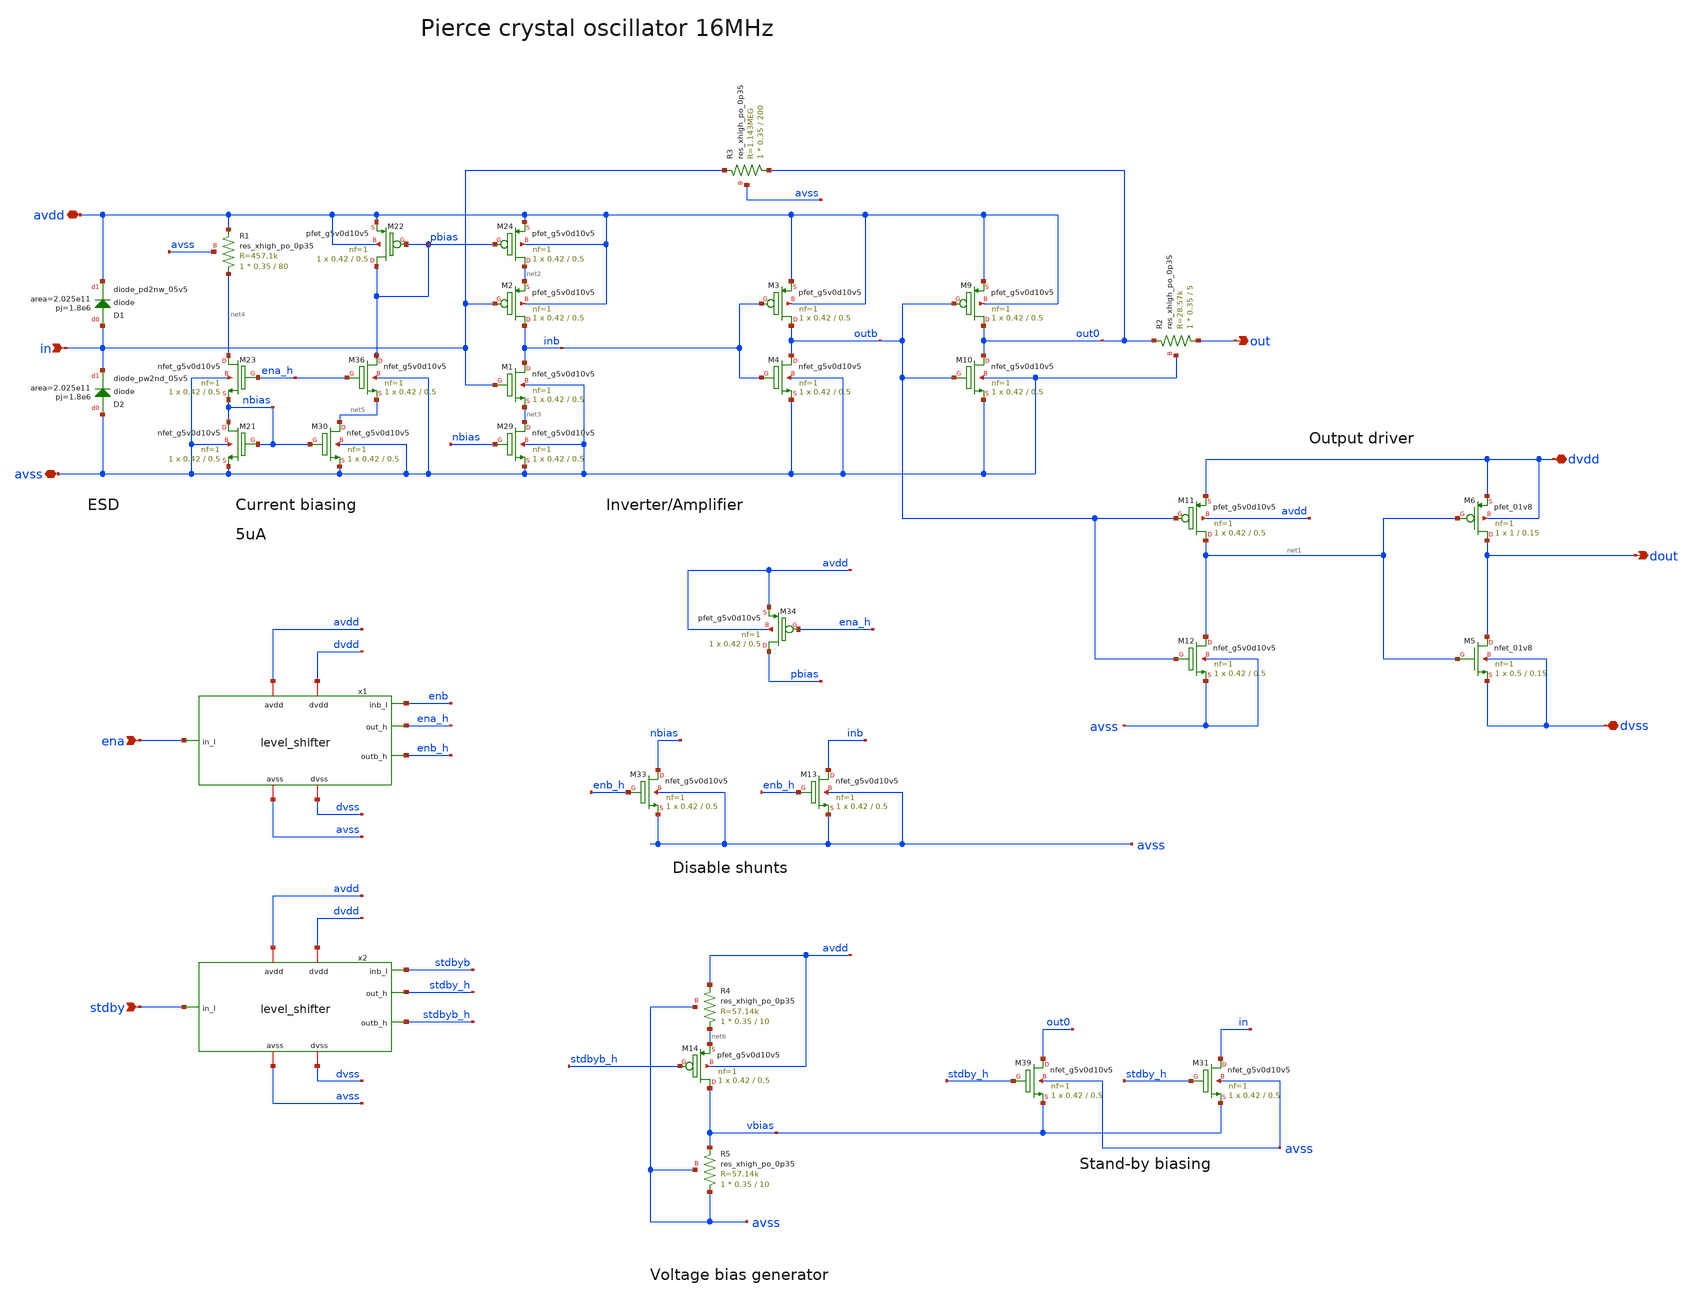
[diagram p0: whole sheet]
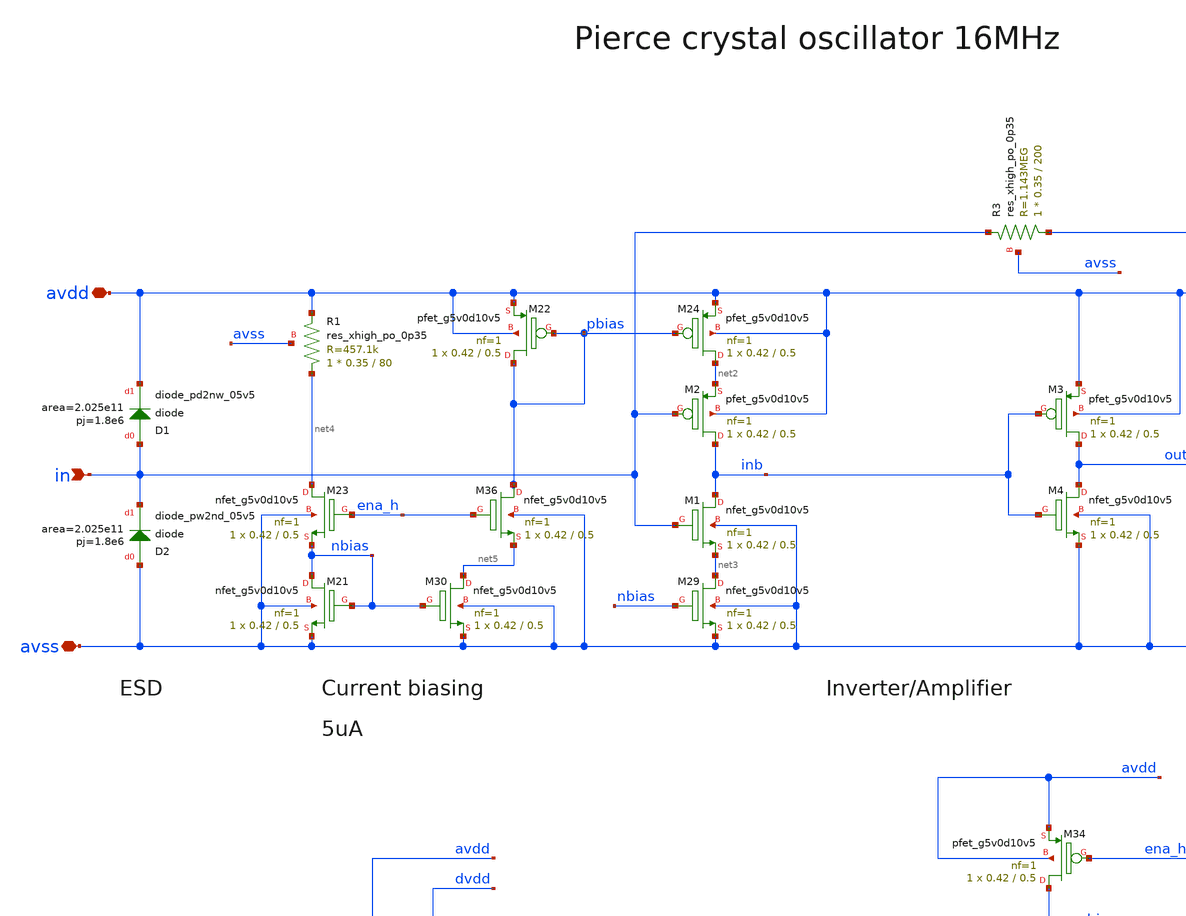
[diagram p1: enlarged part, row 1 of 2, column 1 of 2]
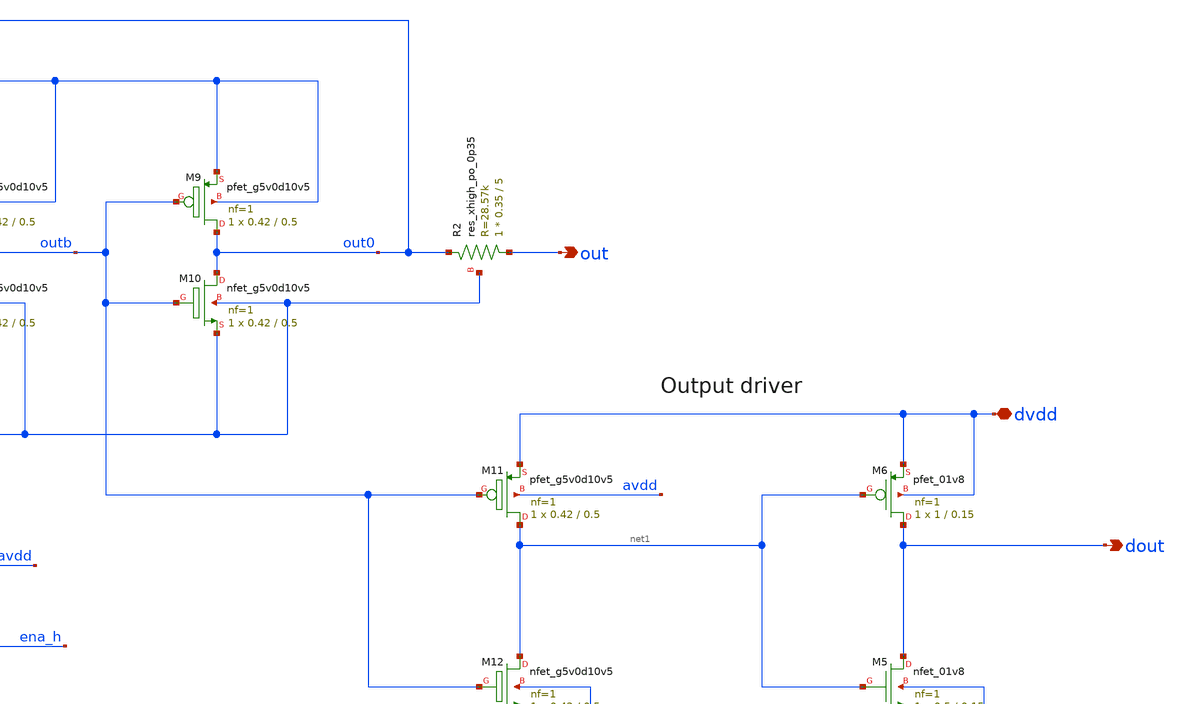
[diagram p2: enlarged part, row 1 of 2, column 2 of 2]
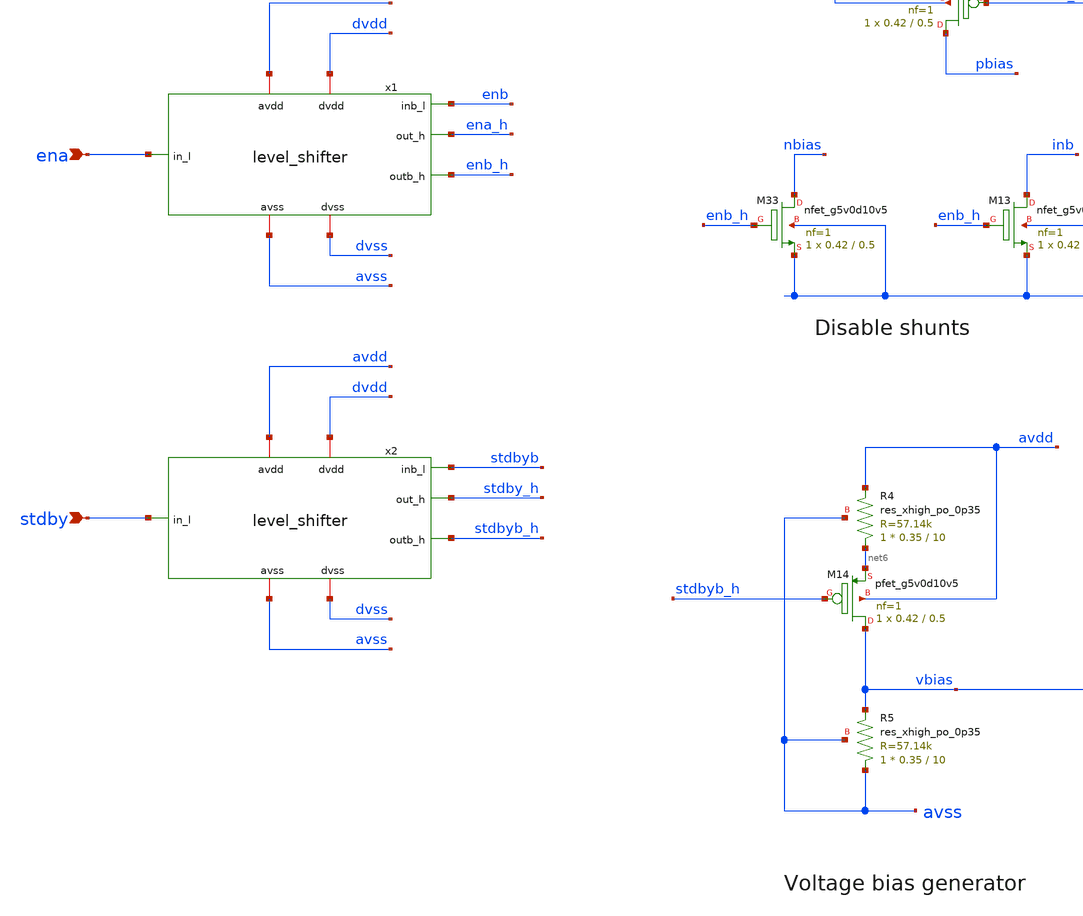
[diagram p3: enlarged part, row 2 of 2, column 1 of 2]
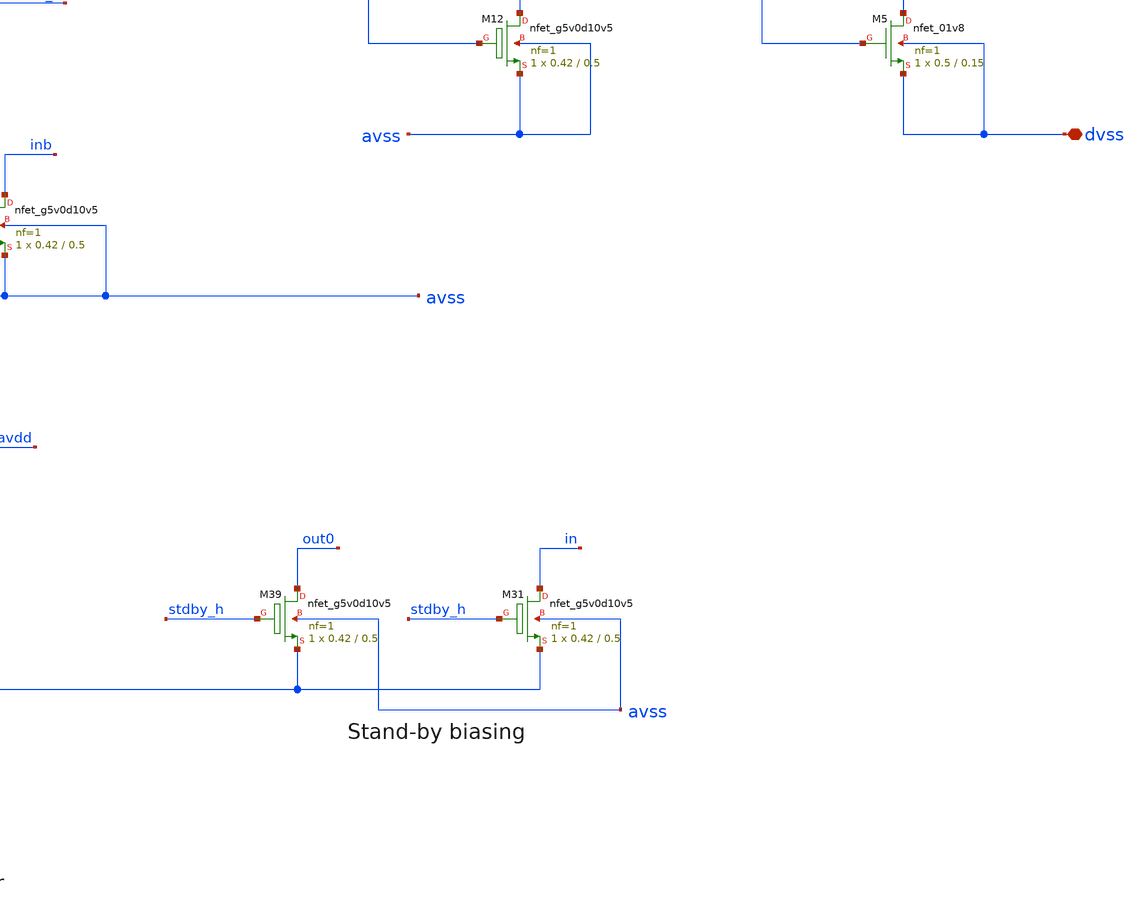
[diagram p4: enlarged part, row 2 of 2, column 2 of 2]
** sch_path: xschem/sky130_ef_ip__xtal_osc_16M.sch
**.subckt sky130_ef_ip__xtal_osc_16M in out avdd avss dvss dvdd ena dout stdby
*.ipin in
*.opin out
*.iopin avdd
*.iopin avss
*.iopin dvss
*.iopin dvdd
*.ipin ena
*.opin dout
*.ipin stdby
XM1 inb in net3 avss sky130_fd_pr__nfet_g5v0d10v5 L=0.5 W=0.42 nf=1 ad='int((nf+1)/2) * W/nf * 0.29'
+ as='int((nf+2)/2) * W/nf * 0.29' pd='2*int((nf+1)/2) * (W/nf + 0.29)' ps='2*int((nf+2)/2) * (W/nf + 0.29)'
+ nrd='0.29 / W' nrs='0.29 / W' sa=0 sb=0 sd=0 mult=1 m=1
XM2 inb in net2 avdd sky130_fd_pr__pfet_g5v0d10v5 L=0.5 W=0.42 nf=1 ad='int((nf+1)/2) * W/nf * 0.29'
+ as='int((nf+2)/2) * W/nf * 0.29' pd='2*int((nf+1)/2) * (W/nf + 0.29)' ps='2*int((nf+2)/2) * (W/nf + 0.29)'
+ nrd='0.29 / W' nrs='0.29 / W' sa=0 sb=0 sd=0 mult=1 m=1
XM3 outb inb avdd avdd sky130_fd_pr__pfet_g5v0d10v5 L=0.5 W=0.42 nf=1 ad='int((nf+1)/2) * W/nf * 0.29'
+ as='int((nf+2)/2) * W/nf * 0.29' pd='2*int((nf+1)/2) * (W/nf + 0.29)' ps='2*int((nf+2)/2) * (W/nf + 0.29)'
+ nrd='0.29 / W' nrs='0.29 / W' sa=0 sb=0 sd=0 mult=1 m=1
XM4 outb inb avss avss sky130_fd_pr__nfet_g5v0d10v5 L=0.5 W=0.42 nf=1 ad='int((nf+1)/2) * W/nf * 0.29'
+ as='int((nf+2)/2) * W/nf * 0.29' pd='2*int((nf+1)/2) * (W/nf + 0.29)' ps='2*int((nf+2)/2) * (W/nf + 0.29)'
+ nrd='0.29 / W' nrs='0.29 / W' sa=0 sb=0 sd=0 mult=1 m=1
XM5 dout net1 dvss dvss sky130_fd_pr__nfet_01v8 L=0.15 W=0.5 nf=1 ad='int((nf+1)/2) * W/nf * 0.29' as='int((nf+2)/2) * W/nf * 0.29'
+ pd='2*int((nf+1)/2) * (W/nf + 0.29)' ps='2*int((nf+2)/2) * (W/nf + 0.29)' nrd='0.29 / W' nrs='0.29 / W'
+ sa=0 sb=0 sd=0 mult=1 m=1
XM6 dout net1 dvdd dvdd sky130_fd_pr__pfet_01v8 L=0.15 W=1 nf=1 ad='int((nf+1)/2) * W/nf * 0.29' as='int((nf+2)/2) * W/nf * 0.29'
+ pd='2*int((nf+1)/2) * (W/nf + 0.29)' ps='2*int((nf+2)/2) * (W/nf + 0.29)' nrd='0.29 / W' nrs='0.29 / W'
+ sa=0 sb=0 sd=0 mult=1 m=1
XR3 out0 in avss sky130_fd_pr__res_xhigh_po_0p35 L=200 mult=1 m=1
XM9 out0 outb avdd avdd sky130_fd_pr__pfet_g5v0d10v5 L=0.5 W=0.42 nf=1 ad='int((nf+1)/2) * W/nf * 0.29'
+ as='int((nf+2)/2) * W/nf * 0.29' pd='2*int((nf+1)/2) * (W/nf + 0.29)' ps='2*int((nf+2)/2) * (W/nf + 0.29)'
+ nrd='0.29 / W' nrs='0.29 / W' sa=0 sb=0 sd=0 mult=1 m=1
XM10 out0 outb avss avss sky130_fd_pr__nfet_g5v0d10v5 L=0.5 W=0.42 nf=1 ad='int((nf+1)/2) * W/nf * 0.29'
+ as='int((nf+2)/2) * W/nf * 0.29' pd='2*int((nf+1)/2) * (W/nf + 0.29)' ps='2*int((nf+2)/2) * (W/nf + 0.29)'
+ nrd='0.29 / W' nrs='0.29 / W' sa=0 sb=0 sd=0 mult=1 m=1
XM11 net1 outb dvdd avdd sky130_fd_pr__pfet_g5v0d10v5 L=0.5 W=0.42 nf=1 ad='int((nf+1)/2) * W/nf * 0.29'
+ as='int((nf+2)/2) * W/nf * 0.29' pd='2*int((nf+1)/2) * (W/nf + 0.29)' ps='2*int((nf+2)/2) * (W/nf + 0.29)'
+ nrd='0.29 / W' nrs='0.29 / W' sa=0 sb=0 sd=0 mult=1 m=1
XM12 net1 outb avss avss sky130_fd_pr__nfet_g5v0d10v5 L=0.5 W=0.42 nf=1 ad='int((nf+1)/2) * W/nf * 0.29'
+ as='int((nf+2)/2) * W/nf * 0.29' pd='2*int((nf+1)/2) * (W/nf + 0.29)' ps='2*int((nf+2)/2) * (W/nf + 0.29)'
+ nrd='0.29 / W' nrs='0.29 / W' sa=0 sb=0 sd=0 mult=1 m=1
XD1 in avdd sky130_fd_pr__diode_pd2nw_05v5 area=2.025e11 pj=1.8e6
XD2 avss in sky130_fd_pr__diode_pw2nd_05v5 area=2.025e11 pj=1.8e6
XM24 net2 pbias avdd avdd sky130_fd_pr__pfet_g5v0d10v5 L=0.5 W=0.42 nf=1 ad='int((nf+1)/2) * W/nf * 0.29'
+ as='int((nf+2)/2) * W/nf * 0.29' pd='2*int((nf+1)/2) * (W/nf + 0.29)' ps='2*int((nf+2)/2) * (W/nf + 0.29)'
+ nrd='0.29 / W' nrs='0.29 / W' sa=0 sb=0 sd=0 mult=1 m=1
XM29 net3 nbias avss avss sky130_fd_pr__nfet_g5v0d10v5 L=0.5 W=0.42 nf=1 ad='int((nf+1)/2) * W/nf * 0.29'
+ as='int((nf+2)/2) * W/nf * 0.29' pd='2*int((nf+1)/2) * (W/nf + 0.29)' ps='2*int((nf+2)/2) * (W/nf + 0.29)'
+ nrd='0.29 / W' nrs='0.29 / W' sa=0 sb=0 sd=0 mult=1 m=1
XM21 nbias nbias avss avss sky130_fd_pr__nfet_g5v0d10v5 L=0.5 W=0.42 nf=1 ad='int((nf+1)/2) * W/nf * 0.29'
+ as='int((nf+2)/2) * W/nf * 0.29' pd='2*int((nf+1)/2) * (W/nf + 0.29)' ps='2*int((nf+2)/2) * (W/nf + 0.29)'
+ nrd='0.29 / W' nrs='0.29 / W' sa=0 sb=0 sd=0 mult=1 m=1
XM22 pbias pbias avdd avdd sky130_fd_pr__pfet_g5v0d10v5 L=0.5 W=0.42 nf=1 ad='int((nf+1)/2) * W/nf * 0.29'
+ as='int((nf+2)/2) * W/nf * 0.29' pd='2*int((nf+1)/2) * (W/nf + 0.29)' ps='2*int((nf+2)/2) * (W/nf + 0.29)'
+ nrd='0.29 / W' nrs='0.29 / W' sa=0 sb=0 sd=0 mult=1 m=1
XR1 net4 avdd avss sky130_fd_pr__res_xhigh_po_0p35 L=80 mult=1 m=1
XM23 net4 ena_h nbias avss sky130_fd_pr__nfet_g5v0d10v5 L=0.5 W=0.42 nf=1 ad='int((nf+1)/2) * W/nf * 0.29'
+ as='int((nf+2)/2) * W/nf * 0.29' pd='2*int((nf+1)/2) * (W/nf + 0.29)' ps='2*int((nf+2)/2) * (W/nf + 0.29)'
+ nrd='0.29 / W' nrs='0.29 / W' sa=0 sb=0 sd=0 mult=1 m=1
XM30 net5 nbias avss avss sky130_fd_pr__nfet_g5v0d10v5 L=0.5 W=0.42 nf=1 ad='int((nf+1)/2) * W/nf * 0.29'
+ as='int((nf+2)/2) * W/nf * 0.29' pd='2*int((nf+1)/2) * (W/nf + 0.29)' ps='2*int((nf+2)/2) * (W/nf + 0.29)'
+ nrd='0.29 / W' nrs='0.29 / W' sa=0 sb=0 sd=0 mult=1 m=1
XM31 in stdby_h vbias avss sky130_fd_pr__nfet_g5v0d10v5 L=0.5 W=0.42 nf=1 ad='int((nf+1)/2) * W/nf * 0.29'
+ as='int((nf+2)/2) * W/nf * 0.29' pd='2*int((nf+1)/2) * (W/nf + 0.29)' ps='2*int((nf+2)/2) * (W/nf + 0.29)'
+ nrd='0.29 / W' nrs='0.29 / W' sa=0 sb=0 sd=0 mult=1 m=1
XM33 nbias enb_h avss avss sky130_fd_pr__nfet_g5v0d10v5 L=0.5 W=0.42 nf=1 ad='int((nf+1)/2) * W/nf * 0.29'
+ as='int((nf+2)/2) * W/nf * 0.29' pd='2*int((nf+1)/2) * (W/nf + 0.29)' ps='2*int((nf+2)/2) * (W/nf + 0.29)'
+ nrd='0.29 / W' nrs='0.29 / W' sa=0 sb=0 sd=0 mult=1 m=1
XM34 pbias ena_h avdd avdd sky130_fd_pr__pfet_g5v0d10v5 L=0.5 W=0.42 nf=1 ad='int((nf+1)/2) * W/nf * 0.29'
+ as='int((nf+2)/2) * W/nf * 0.29' pd='2*int((nf+1)/2) * (W/nf + 0.29)' ps='2*int((nf+2)/2) * (W/nf + 0.29)'
+ nrd='0.29 / W' nrs='0.29 / W' sa=0 sb=0 sd=0 mult=1 m=1
XM36 pbias ena_h net5 avss sky130_fd_pr__nfet_g5v0d10v5 L=0.5 W=0.42 nf=1 ad='int((nf+1)/2) * W/nf * 0.29'
+ as='int((nf+2)/2) * W/nf * 0.29' pd='2*int((nf+1)/2) * (W/nf + 0.29)' ps='2*int((nf+2)/2) * (W/nf + 0.29)'
+ nrd='0.29 / W' nrs='0.29 / W' sa=0 sb=0 sd=0 mult=1 m=1
XM13 inb enb_h avss avss sky130_fd_pr__nfet_g5v0d10v5 L=0.5 W=0.42 nf=1 ad='int((nf+1)/2) * W/nf * 0.29'
+ as='int((nf+2)/2) * W/nf * 0.29' pd='2*int((nf+1)/2) * (W/nf + 0.29)' ps='2*int((nf+2)/2) * (W/nf + 0.29)'
+ nrd='0.29 / W' nrs='0.29 / W' sa=0 sb=0 sd=0 mult=1 m=1
XR2 out out0 avss sky130_fd_pr__res_xhigh_po_0p35 L=5 mult=1 m=1
XR5 avss vbias avss sky130_fd_pr__res_xhigh_po_0p35 L=10 mult=1 m=1
XM14 vbias stdbyb_h net6 avdd sky130_fd_pr__pfet_g5v0d10v5 L=0.5 W=0.42 nf=1 ad='int((nf+1)/2) * W/nf * 0.29'
+ as='int((nf+2)/2) * W/nf * 0.29' pd='2*int((nf+1)/2) * (W/nf + 0.29)' ps='2*int((nf+2)/2) * (W/nf + 0.29)'
+ nrd='0.29 / W' nrs='0.29 / W' sa=0 sb=0 sd=0 mult=1 m=1
XM39 out0 stdby_h vbias avss sky130_fd_pr__nfet_g5v0d10v5 L=0.5 W=0.42 nf=1 ad='int((nf+1)/2) * W/nf * 0.29'
+ as='int((nf+2)/2) * W/nf * 0.29' pd='2*int((nf+1)/2) * (W/nf + 0.29)' ps='2*int((nf+2)/2) * (W/nf + 0.29)'
+ nrd='0.29 / W' nrs='0.29 / W' sa=0 sb=0 sd=0 mult=1 m=1
XR4 net6 avdd avss sky130_fd_pr__res_xhigh_po_0p35 L=10 mult=1 m=1
x1 dvdd ena_h avdd enb_h ena dvss avss enb level_shifter
x2 dvdd stdby_h avdd stdbyb_h stdby dvss avss stdbyb level_shifter
**.ends

* expanding   symbol:  level_shifter.sym # of pins=8
** sym_path: xschem/level_shifter.sym
** sch_path: xschem/level_shifter.sch
.subckt level_shifter dvdd out_h avdd outb_h in_l dvss avss inb_l
*.ipin in_l
*.iopin dvdd
*.iopin avdd
*.iopin dvss
*.iopin avss
*.opin out_h
*.opin outb_h
*.opin inb_l
XM7 inb_l in_l dvdd dvdd sky130_fd_pr__pfet_01v8 L=0.15 W=1 nf=1 ad='int((nf+1)/2) * W/nf * 0.29' as='int((nf+2)/2) * W/nf * 0.29'
+ pd='2*int((nf+1)/2) * (W/nf + 0.29)' ps='2*int((nf+2)/2) * (W/nf + 0.29)' nrd='0.29 / W' nrs='0.29 / W'
+ sa=0 sb=0 sd=0 mult=1 m=1
XM8 inb_l in_l dvss dvss sky130_fd_pr__nfet_01v8 L=0.15 W=1 nf=1 ad='int((nf+1)/2) * W/nf * 0.29' as='int((nf+2)/2) * W/nf * 0.29'
+ pd='2*int((nf+1)/2) * (W/nf + 0.29)' ps='2*int((nf+2)/2) * (W/nf + 0.29)' nrd='0.29 / W' nrs='0.29 / W'
+ sa=0 sb=0 sd=0 mult=1 m=1
XM15 out_h outb_h net1 avdd sky130_fd_pr__pfet_g5v0d10v5 L=0.5 W=0.42 nf=1 ad='int((nf+1)/2) * W/nf * 0.29'
+ as='int((nf+2)/2) * W/nf * 0.29' pd='2*int((nf+1)/2) * (W/nf + 0.29)' ps='2*int((nf+2)/2) * (W/nf + 0.29)'
+ nrd='0.29 / W' nrs='0.29 / W' sa=0 sb=0 sd=0 mult=1 m=1
XM16 outb_h out_h net2 avdd sky130_fd_pr__pfet_g5v0d10v5 L=0.5 W=0.42 nf=1 ad='int((nf+1)/2) * W/nf * 0.29'
+ as='int((nf+2)/2) * W/nf * 0.29' pd='2*int((nf+1)/2) * (W/nf + 0.29)' ps='2*int((nf+2)/2) * (W/nf + 0.29)'
+ nrd='0.29 / W' nrs='0.29 / W' sa=0 sb=0 sd=0 mult=1 m=1
XM17 outb_h in_l avss avss sky130_fd_pr__nfet_g5v0d10v5 L=0.5 W=0.42 nf=1 ad='int((nf+1)/2) * W/nf * 0.29'
+ as='int((nf+2)/2) * W/nf * 0.29' pd='2*int((nf+1)/2) * (W/nf + 0.29)' ps='2*int((nf+2)/2) * (W/nf + 0.29)'
+ nrd='0.29 / W' nrs='0.29 / W' sa=0 sb=0 sd=0 mult=1 m=1
XM18 out_h inb_l avss avss sky130_fd_pr__nfet_g5v0d10v5 L=0.5 W=0.42 nf=1 ad='int((nf+1)/2) * W/nf * 0.29'
+ as='int((nf+2)/2) * W/nf * 0.29' pd='2*int((nf+1)/2) * (W/nf + 0.29)' ps='2*int((nf+2)/2) * (W/nf + 0.29)'
+ nrd='0.29 / W' nrs='0.29 / W' sa=0 sb=0 sd=0 mult=1 m=1
XM19 net1 out_h avdd avdd sky130_fd_pr__pfet_g5v0d10v5 L=0.5 W=0.42 nf=1 ad='int((nf+1)/2) * W/nf * 0.29'
+ as='int((nf+2)/2) * W/nf * 0.29' pd='2*int((nf+1)/2) * (W/nf + 0.29)' ps='2*int((nf+2)/2) * (W/nf + 0.29)'
+ nrd='0.29 / W' nrs='0.29 / W' sa=0 sb=0 sd=0 mult=1 m=1
XM20 net2 outb_h avdd avdd sky130_fd_pr__pfet_g5v0d10v5 L=0.5 W=0.42 nf=1 ad='int((nf+1)/2) * W/nf * 0.29'
+ as='int((nf+2)/2) * W/nf * 0.29' pd='2*int((nf+1)/2) * (W/nf + 0.29)' ps='2*int((nf+2)/2) * (W/nf + 0.29)'
+ nrd='0.29 / W' nrs='0.29 / W' sa=0 sb=0 sd=0 mult=1 m=1
.ends

.end
